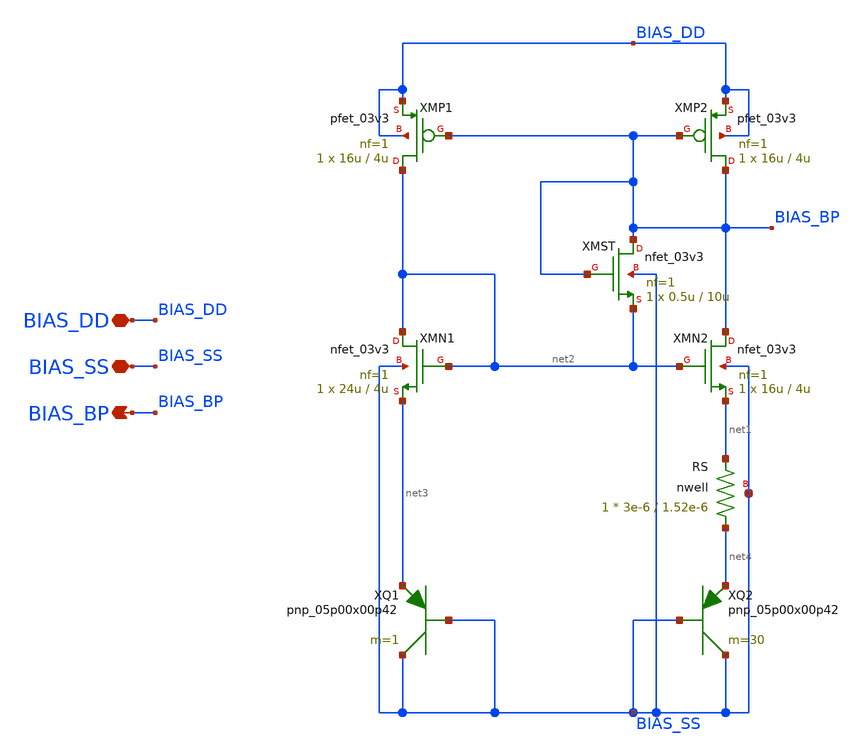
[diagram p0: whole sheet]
** sch_path: Design_Files/IC Design/Schematic/POWER_BLOCKS/BIAS/BIAS.sch
**.subckt BIAS BIAS_DD BIAS_SS BIAS_BP
*.iopin BIAS_DD
*.iopin BIAS_SS
*.opin BIAS_BP
XMN2 BIAS_BP net2 net1 BIAS_SS nfet_03v3 L=4u W=16u nf=1 ad='int((nf+1)/2) * W/nf * 0.18u' as='int((nf+2)/2) * W/nf * 0.18u'
+ pd='2*int((nf+1)/2) * (W/nf + 0.18u)' ps='2*int((nf+2)/2) * (W/nf + 0.18u)' nrd='0.18u / W' nrs='0.18u / W'
+ sa=0 sb=0 sd=0 m=1
XMP2 BIAS_BP BIAS_BP BIAS_DD BIAS_DD pfet_03v3 L=4u W=16u nf=1 ad='int((nf+1)/2) * W/nf * 0.18u' as='int((nf+2)/2) * W/nf * 0.18u'
+ pd='2*int((nf+1)/2) * (W/nf + 0.18u)' ps='2*int((nf+2)/2) * (W/nf + 0.18u)' nrd='0.18u / W' nrs='0.18u / W'
+ sa=0 sb=0 sd=0 m=1
XMN1 net2 net2 net3 BIAS_SS nfet_03v3 L=4u W=24u nf=1 ad='int((nf+1)/2) * W/nf * 0.18u' as='int((nf+2)/2) * W/nf * 0.18u'
+ pd='2*int((nf+1)/2) * (W/nf + 0.18u)' ps='2*int((nf+2)/2) * (W/nf + 0.18u)' nrd='0.18u / W' nrs='0.18u / W'
+ sa=0 sb=0 sd=0 m=1
XMP1 net2 BIAS_BP BIAS_DD BIAS_DD pfet_03v3 L=4u W=16u nf=1 ad='int((nf+1)/2) * W/nf * 0.18u' as='int((nf+2)/2) * W/nf * 0.18u'
+ pd='2*int((nf+1)/2) * (W/nf + 0.18u)' ps='2*int((nf+2)/2) * (W/nf + 0.18u)' nrd='0.18u / W' nrs='0.18u / W'
+ sa=0 sb=0 sd=0 m=1
XMST BIAS_BP BIAS_BP net2 BIAS_SS nfet_03v3 L=10u W=0.5u nf=1 ad='int((nf+1)/2) * W/nf * 0.18u' as='int((nf+2)/2) * W/nf * 0.18u'
+ pd='2*int((nf+1)/2) * (W/nf + 0.18u)' ps='2*int((nf+2)/2) * (W/nf + 0.18u)' nrd='0.18u / W' nrs='0.18u / W'
+ sa=0 sb=0 sd=0 m=1
XQ1 BIAS_SS BIAS_SS net3 pnp_05p00x00p42 m=1 par=1
XQ2 BIAS_SS BIAS_SS net4 pnp_05p00x00p42 m=30 par=30
XRS net4 net1 BIAS_SS nwell r_width=3e-6 r_length=1.52e-6 m=1
**.ends
.end
